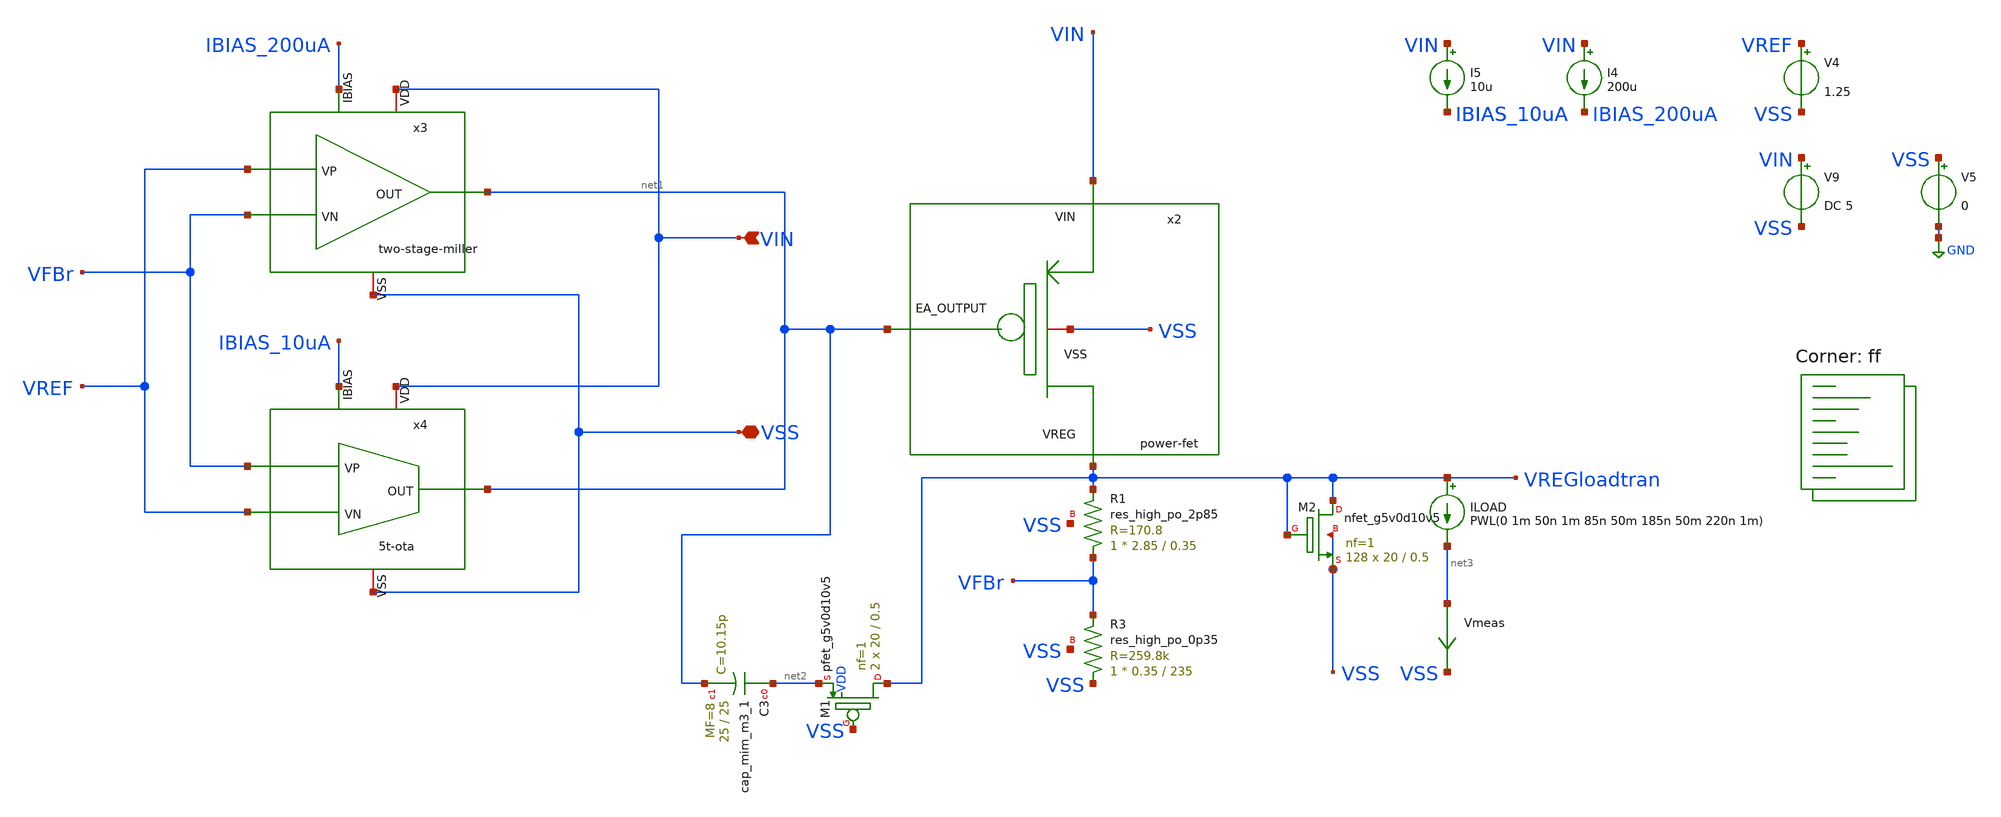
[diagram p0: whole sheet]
** sch_path: bandgap/testbench/tb_tran_settling-time.sch
**.subckt tb_tran_settling-time VIN VSS
*.ipin VIN
*.iopin VSS
x2 VIN VSS net1 VREGloadtran power-fet
XR3 VSS VFBr VSS sky130_fd_pr__res_high_po_0p35 L=235 mult=1 m=1
XR1 VFBr VREGloadtran VSS sky130_fd_pr__res_high_po_2p85 L=0.35 mult=1 m=1
x3 VIN net1 VREF VFBr IBIAS_200uA VSS two-stage-miller
x4 VIN net1 IBIAS_10uA VREF VFBr VSS 5t-ota
I4 VIN IBIAS_200uA 200u
ILOAD VREGloadtran net3 PWL(0 1m 50n 1m 85n 50m 185n 50m 220n 1m)
V4 VREF VSS 1.25
V5 VSS GND 0
V9 VIN VSS DC 5
I5 VIN IBIAS_10uA 10u
XM2 VREGloadtran VREGloadtran VSS VSS sky130_fd_pr__nfet_g5v0d10v5 L=0.5 W=20 nf=1 ad='int((nf+1)/2) * W/nf * 0.29'
+ as='int((nf+2)/2) * W/nf * 0.29' pd='2*int((nf+1)/2) * (W/nf + 0.29)' ps='2*int((nf+2)/2) * (W/nf + 0.29)'
+ nrd='0.29 / W' nrs='0.29 / W' sa=0 sb=0 sd=0 mult=128 m=128
XC3 net2 net1 sky130_fd_pr__cap_mim_m3_1 W=25 L=25 MF=8 m=8
XM1 VREGloadtran VSS net2 VDD sky130_fd_pr__pfet_g5v0d10v5 L=0.5 W=20 nf=1 ad='int((nf+1)/2) * W/nf * 0.29'
+ as='int((nf+2)/2) * W/nf * 0.29' pd='2*int((nf+1)/2) * (W/nf + 0.29)' ps='2*int((nf+2)/2) * (W/nf + 0.29)'
+ nrd='0.29 / W' nrs='0.29 / W' sa=0 sb=0 sd=0 mult=2 m=2
Vmeas net3 VSS 0
.save i(vmeas)
**** begin user architecture code



.temp 175
.control

tran 1p 1u

* Nominal output voltage (from regulation region)
let Vout_nom = 1.25
let Vout_95  = 0.95*Vout_nom

* Find Vin where Vout crosses 95%
meas dc Vin_do find v(vin) when v(vreg)=Vout_95

* Measure Vout at that Vin (for completeness)
meas dc Vout_do find v(vreg) when v(vreg)=Vout_95

* Compute dropout voltage
let Vdo = Vin_do - Vout_do

* Compute overshoot, undershoot and peak-to-peak voltage
meas tran Vout_max MAX v(VREGloadtran)
meas tran Vout_min MIN v(VREGloadtran)
let vpp = Vout_max - Vout_min

*Compute PSRR
meas ac psrr_dc  param= -20*log10(mag(v(VREGac)))  at=1
meas ac psrr_100k  param= -20*log10(mag(v(VREGac)))  at=100k
meas ac psrr_1M  param= -20*log10(mag(v(VREGaz)))  at=1Meg

* --- Settling Time Measurement Block ---
let v_final = 1.25  ; Target Vout
let tol = 0.01 * v_final
let hi_bound = v_final + tol
let lo_bound = v_final - tol

* 1. FIXED TRIGGER: We know the PWL starts the rise at 50ns
let t_trigger = 50n

* 2. Find the LAST time the signal was outside the tolerance band
* We measure after the step occurs (after 50ns)
meas tran t_last_hi WHEN v(VREGloadtran)=hi_bound FALL=LAST
meas tran t_last_lo WHEN v(VREGloadtran)=lo_bound RISE=LAST

* 3. Calculate Settling Time
* Ensure we only look at crossings that happened AFTER the trigger
let t_settle_end = max(t_last_hi, t_last_lo)
let settling_time = t_settle_end - t_trigger

print settling_time


print Vin_do Vout_do Vdo
print Vout_max Vout_min Vpp
plot VREGloadtran
plot VREGloadtran2
plot VREG
plot VIN
plot I(Vmeas)

.endc


.lib $::SKYWATER_MODELS/sky130.lib.spice ff
**** end user architecture code
**.ends
.GLOBAL GND
.end
